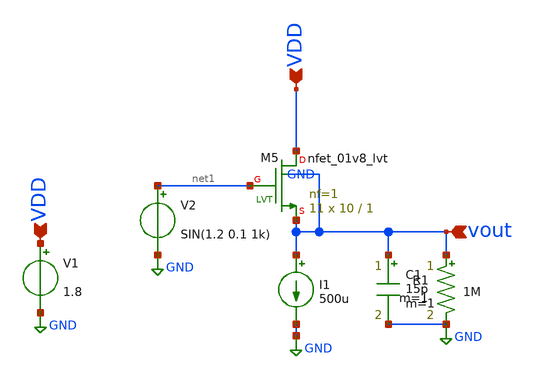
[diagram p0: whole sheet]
** sch_path: xschem/EA/commondrain.sch
**.subckt commondrain VDD VDD vout
*.ipin VDD
*.ipin VDD
*.ipin vout
XM5 VDD net1 vout GND sky130_fd_pr__nfet_01v8_lvt L=1 W=10 nf=1 ad='int((1 + 1)/2) * 10 / 1 * 0.29' as='int((1 + 2)/2) * 10 / 1 * 0.29'
+ pd='2*int((1 + 1)/2) * (10 / 1 + 0.29)' ps='2*int((1 + 2)/2) * (10 / 1 + 0.29)' nrd='0.29 / 10 ' nrs='0.29 / 10 '
+ sa=0 sb=0 sd=0 mult=11 m=11
I1 vout GND 500u
V2 net1 GND SIN(1.2 0.1 1k)
V1 VDD GND 1.8
R1 vout GND 1M m=1
C1 vout GND 15p m=1
**** begin user architecture code



.lib /usr/local/share/pdk/sky130A/libs.tech/ngspice/sky130.lib.spice tt
.tran 5u 3m
.save all

.control
run
print @m.xm5.msky130_fd_pr__nfet_01v8_lvt[vth]
plot vout title vout

set wr_singlescale
set wr_vecnames
*wrdata /foss/designs/2stageCMOSOpAmp/sim_data/GainvsFreq/gain(max).txt db(vout/v(v+))
*wrdata /foss/designs/2stageCMOSOpAmp/sim_data/sample_waves/a1.3m_f1k_gain700.txt vout
*wrdata /foss/designs/2stageCMOSOpAmp/sim_data/SR/SR.txt vout

.endc


**** end user architecture code
**.ends
.GLOBAL GND
.end
